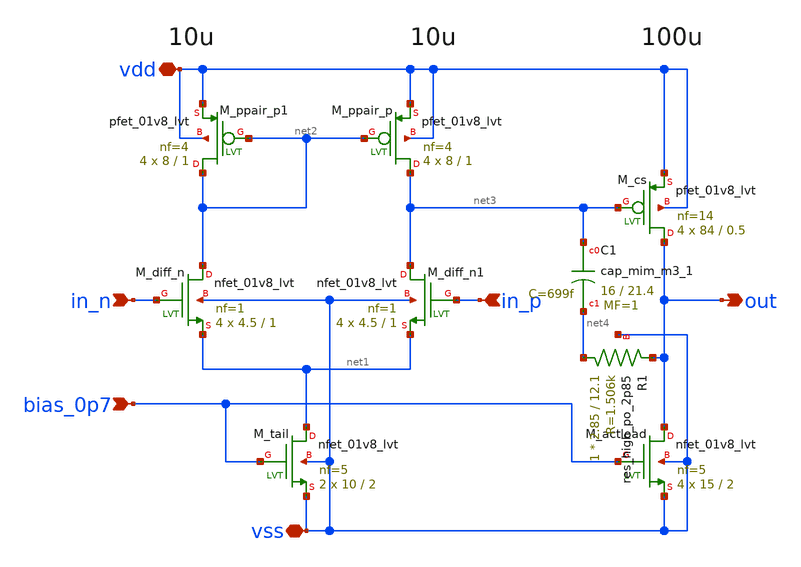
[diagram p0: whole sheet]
** sch_path: design/opamp/opamp_realcomp3_usefinger.sch
**.subckt opamp_realcomp3_usefinger vdd vss in_n in_p out bias_0p7
*.iopin vdd
*.iopin vss
*.ipin in_n
*.ipin in_p
*.opin out
*.ipin bias_0p7
XM_diff_n net2 in_n net1 vss sky130_fd_pr__nfet_01v8_lvt L=1 W=4.5 nf=1 ad='int((nf+1)/2) * W/nf * 0.29'
+ as='int((nf+2)/2) * W/nf * 0.29' pd='2*int((nf+1)/2) * (W/nf + 0.29)' ps='2*int((nf+2)/2) * (W/nf + 0.29)'
+ nrd='0.29 / W' nrs='0.29 / W' sa=0 sb=0 sd=0 mult=4 m=4
XM_diff_n1 net3 in_p net1 vss sky130_fd_pr__nfet_01v8_lvt L=1 W=4.5 nf=1 ad='int((nf+1)/2) * W/nf * 0.29'
+ as='int((nf+2)/2) * W/nf * 0.29' pd='2*int((nf+1)/2) * (W/nf + 0.29)' ps='2*int((nf+2)/2) * (W/nf + 0.29)'
+ nrd='0.29 / W' nrs='0.29 / W' sa=0 sb=0 sd=0 mult=4 m=4
XM_tail net1 bias_0p7 vss vss sky130_fd_pr__nfet_01v8_lvt L=2 W=10 nf=5 ad='int((nf+1)/2) * W/nf * 0.29'
+ as='int((nf+2)/2) * W/nf * 0.29' pd='2*int((nf+1)/2) * (W/nf + 0.29)' ps='2*int((nf+2)/2) * (W/nf + 0.29)'
+ nrd='0.29 / W' nrs='0.29 / W' sa=0 sb=0 sd=0 mult=2 m=2
XM_actload out bias_0p7 vss vss sky130_fd_pr__nfet_01v8_lvt L=2 W=15 nf=5 ad='int((nf+1)/2) * W/nf * 0.29'
+ as='int((nf+2)/2) * W/nf * 0.29' pd='2*int((nf+1)/2) * (W/nf + 0.29)' ps='2*int((nf+2)/2) * (W/nf + 0.29)'
+ nrd='0.29 / W' nrs='0.29 / W' sa=0 sb=0 sd=0 mult=4 m=4
XM_ppair_p net3 net2 vdd vdd sky130_fd_pr__pfet_01v8_lvt L=1 W=8 nf=4 ad='int((nf+1)/2) * W/nf * 0.29'
+ as='int((nf+2)/2) * W/nf * 0.29' pd='2*int((nf+1)/2) * (W/nf + 0.29)' ps='2*int((nf+2)/2) * (W/nf + 0.29)'
+ nrd='0.29 / W' nrs='0.29 / W' sa=0 sb=0 sd=0 mult=4 m=4
XM_ppair_p1 net2 net2 vdd vdd sky130_fd_pr__pfet_01v8_lvt L=1 W=8 nf=4 ad='int((nf+1)/2) * W/nf * 0.29'
+ as='int((nf+2)/2) * W/nf * 0.29' pd='2*int((nf+1)/2) * (W/nf + 0.29)' ps='2*int((nf+2)/2) * (W/nf + 0.29)'
+ nrd='0.29 / W' nrs='0.29 / W' sa=0 sb=0 sd=0 mult=4 m=4
XM_cs out net3 vdd vdd sky130_fd_pr__pfet_01v8_lvt L=0.5 W=84 nf=14 ad='int((nf+1)/2) * W/nf * 0.29'
+ as='int((nf+2)/2) * W/nf * 0.29' pd='2*int((nf+1)/2) * (W/nf + 0.29)' ps='2*int((nf+2)/2) * (W/nf + 0.29)'
+ nrd='0.29 / W' nrs='0.29 / W' sa=0 sb=0 sd=0 mult=4 m=4
XC1 net3 net4 sky130_fd_pr__cap_mim_m3_1 W=16 L=21.4 MF=1 m=1
XR1 net4 out vss sky130_fd_pr__res_high_po_2p85 L=12.1 mult=1 m=1
**.ends
.end
